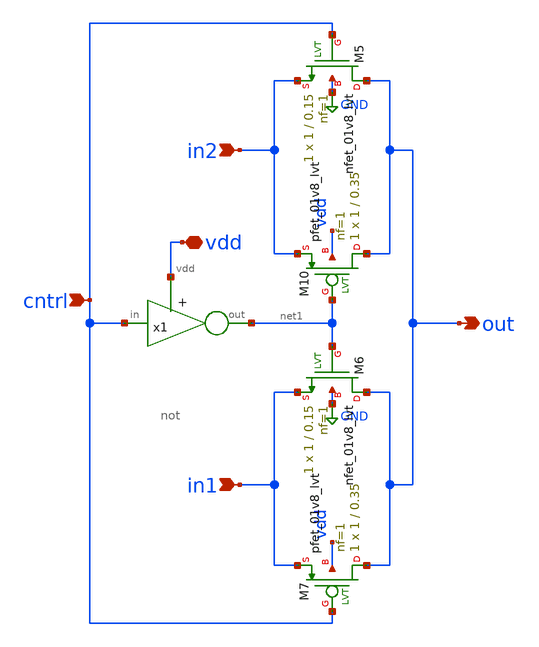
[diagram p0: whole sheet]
** sch_path: designs/subcells/core_conmutator/conmutator.sch
**.subckt conmutator cntrl in2 in1 vdd out
*.ipin cntrl
*.ipin in2
*.ipin in1
*.iopin vdd
*.opin out
x1 vdd cntrl net1 not
XM5 out cntrl in2 GND sky130_fd_pr__nfet_01v8_lvt L=0.15 W=1 nf=1 ad='int((1 + 1)/2) * 1 / 1 * 0.29'
+ as='int((1 + 2)/2) * 1 / 1 * 0.29' pd='2*int((1 + 1)/2) * (1 / 1 + 0.29)' ps='2*int((1 + 2)/2) * (1 / 1 + 0.29)'
+ nrd='0.29 / 1 ' nrs='0.29 / 1 ' sa=0 sb=0 sd=0 mult=1 m=1
XM10 out net1 in2 vdd sky130_fd_pr__pfet_01v8_lvt L=0.35 W=1 nf=1 ad='int((1 + 1)/2) * 1 / 1 * 0.29'
+ as='int((1 + 2)/2) * 1 / 1 * 0.29' pd='2*int((1 + 1)/2) * (1 / 1 + 0.29)' ps='2*int((1 + 2)/2) * (1 / 1 + 0.29)'
+ nrd='0.29 / 1 ' nrs='0.29 / 1 ' sa=0 sb=0 sd=0 mult=1 m=1
XM6 out net1 in1 GND sky130_fd_pr__nfet_01v8_lvt L=0.15 W=1 nf=1 ad='int((1 + 1)/2) * 1 / 1 * 0.29' as='int((1 + 2)/2) * 1 / 1 * 0.29'
+ pd='2*int((1 + 1)/2) * (1 / 1 + 0.29)' ps='2*int((1 + 2)/2) * (1 / 1 + 0.29)' nrd='0.29 / 1 ' nrs='0.29 / 1 '
+ sa=0 sb=0 sd=0 mult=1 m=1
XM7 out cntrl in1 vdd sky130_fd_pr__pfet_01v8_lvt L=0.35 W=1 nf=1 ad='int((1 + 1)/2) * 1 / 1 * 0.29'
+ as='int((1 + 2)/2) * 1 / 1 * 0.29' pd='2*int((1 + 1)/2) * (1 / 1 + 0.29)' ps='2*int((1 + 2)/2) * (1 / 1 + 0.29)'
+ nrd='0.29 / 1 ' nrs='0.29 / 1 ' sa=0 sb=0 sd=0 mult=1 m=1
**.ends

* expanding   symbol:  /foss/designs/spike_130/designs/subcells/core_not/not.sym # of pins=3
** sym_path: designs/subcells/core_not/not.sym
** sch_path: designs/subcells/core_not/not.sch
.subckt not vdd in out
*.ipin in
*.opin out
*.iopin vdd
XM10 out in vdd vdd sky130_fd_pr__pfet_01v8_lvt L=0.35 W=1 nf=1 ad='int((1 + 1)/2) * 1 / 1 * 0.29' as='int((1 + 2)/2) * 1 / 1 * 0.29'
+ pd='2*int((1 + 1)/2) * (1 / 1 + 0.29)' ps='2*int((1 + 2)/2) * (1 / 1 + 0.29)' nrd='0.29 / 1 ' nrs='0.29 / 1 '
+ sa=0 sb=0 sd=0 mult=1 m=1
XM1 out in GND GND sky130_fd_pr__nfet_01v8_lvt L=0.15 W=1 nf=1 ad='int((1 + 1)/2) * 1 / 1 * 0.29' as='int((1 + 2)/2) * 1 / 1 * 0.29'
+ pd='2*int((1 + 1)/2) * (1 / 1 + 0.29)' ps='2*int((1 + 2)/2) * (1 / 1 + 0.29)' nrd='0.29 / 1 ' nrs='0.29 / 1 '
+ sa=0 sb=0 sd=0 mult=1 m=1
.ends

.GLOBAL GND
.end
